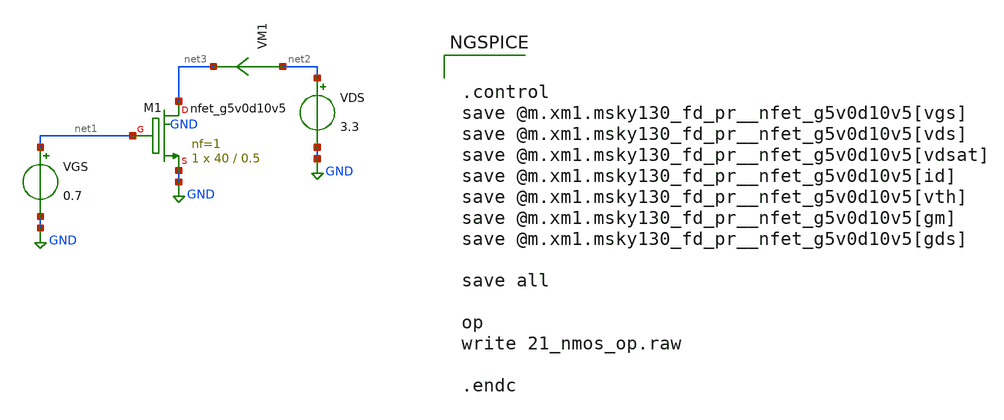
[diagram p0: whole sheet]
** sch_path: xschem/help/21_nmos_op.sch
**.subckt 21_nmos_op
XM1 net3 net1 GND GND sky130_fd_pr__nfet_g5v0d10v5 L=0.5 W=40 nf=1 ad='int((nf+1)/2) * W/nf * 0.29' as='int((nf+2)/2) * W/nf * 0.29'
+ pd='2*int((nf+1)/2) * (W/nf + 0.29)' ps='2*int((nf+2)/2) * (W/nf + 0.29)' nrd='0.29 / W' nrs='0.29 / W'
+ sa=0 sb=0 sd=0 mult=1 m=1
VGS net1 GND 0.7
VDS net2 GND 3.3
VM1 net2 net3 0
.save i(vm1)
**** begin user architecture code

** opencircuitdesign pdks install
.lib $::SKYWATER_MODELS/sky130.lib.spice tt




.control
save @m.xm1.msky130_fd_pr__nfet_g5v0d10v5[vgs]
save @m.xm1.msky130_fd_pr__nfet_g5v0d10v5[vds]
save @m.xm1.msky130_fd_pr__nfet_g5v0d10v5[vdsat]
save @m.xm1.msky130_fd_pr__nfet_g5v0d10v5[id]
save @m.xm1.msky130_fd_pr__nfet_g5v0d10v5[vth]
save @m.xm1.msky130_fd_pr__nfet_g5v0d10v5[gm]
save @m.xm1.msky130_fd_pr__nfet_g5v0d10v5[gds]

save all

op
write 21_nmos_op.raw

.endc


**** end user architecture code
**.ends
.GLOBAL GND
.end
